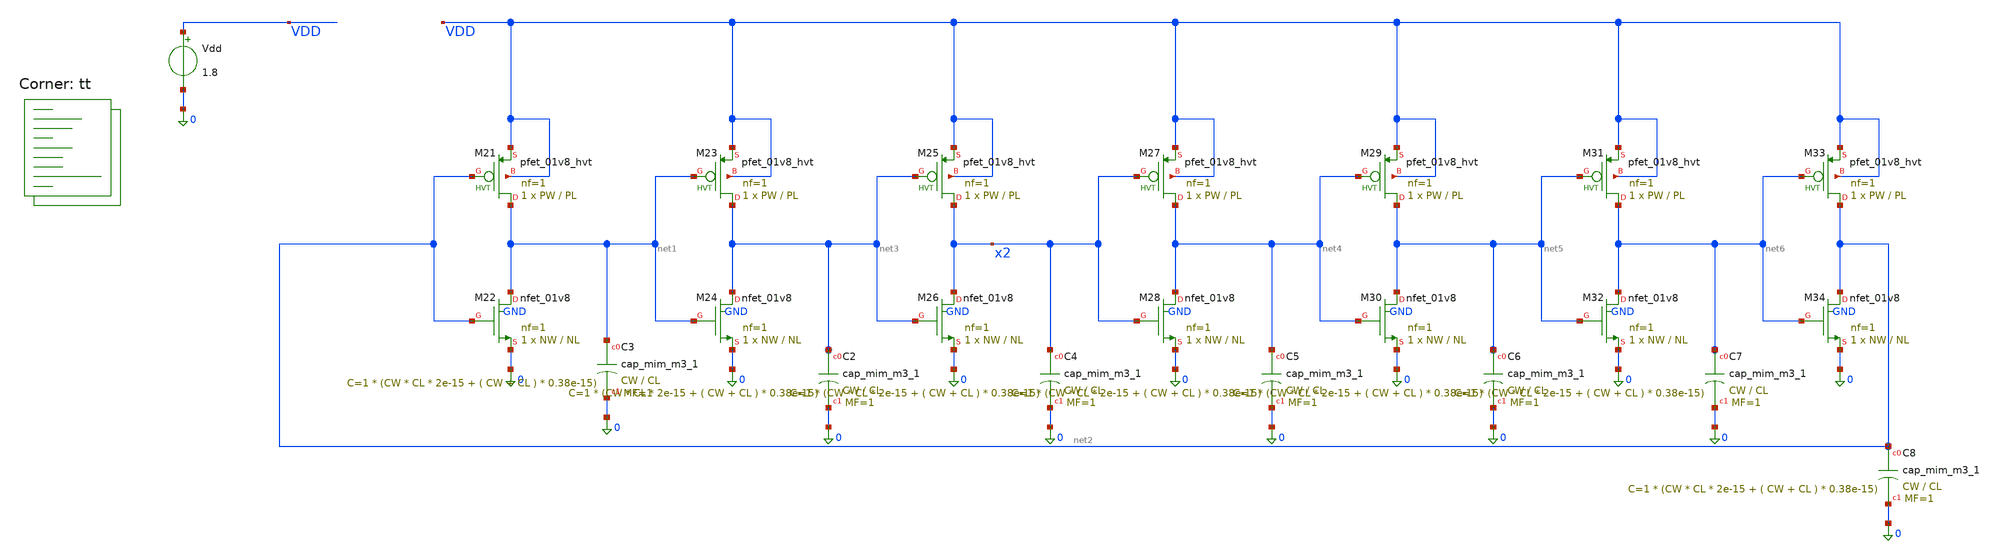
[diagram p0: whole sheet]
** sch_path: schem/ring_osc_trans_analysis_tb.sch
**.subckt ring_osc_trans_analysis_tb
XM21 net1 net2 VDD VDD sky130_fd_pr__pfet_01v8_hvt L=PL W=PW nf=1 ad='int((1 + 1)/2) * PW / 1 * 0.29'
+ as='int((1 + 2)/2) * PW / 1 * 0.29' pd='2*int((1 + 1)/2) * (PW / 1 + 0.29)' ps='2*int((1 + 2)/2) * (PW / 1 + 0.29)'
+ nrd='0.29 / PW ' nrs='0.29 / PW ' sa=0 sb=0 sd=0 mult=1 m=1
XM22 net1 net2 0 GND sky130_fd_pr__nfet_01v8 L=NL W=NW nf=1 ad='int((1 + 1)/2) * NW / 1 * 0.29' as='int((1 + 2)/2) * NW / 1 * 0.29'
+ pd='2*int((1 + 1)/2) * (NW / 1 + 0.29)' ps='2*int((1 + 2)/2) * (NW / 1 + 0.29)' nrd='0.29 / NW ' nrs='0.29 / NW '
+ sa=0 sb=0 sd=0 mult=1 m=1
XM23 net3 net1 VDD VDD sky130_fd_pr__pfet_01v8_hvt L=PL W=PW nf=1 ad='int((1 + 1)/2) * PW / 1 * 0.29'
+ as='int((1 + 2)/2) * PW / 1 * 0.29' pd='2*int((1 + 1)/2) * (PW / 1 + 0.29)' ps='2*int((1 + 2)/2) * (PW / 1 + 0.29)'
+ nrd='0.29 / PW ' nrs='0.29 / PW ' sa=0 sb=0 sd=0 mult=1 m=1
XM24 net3 net1 0 GND sky130_fd_pr__nfet_01v8 L=NL W=NW nf=1 ad='int((1 + 1)/2) * NW / 1 * 0.29' as='int((1 + 2)/2) * NW / 1 * 0.29'
+ pd='2*int((1 + 1)/2) * (NW / 1 + 0.29)' ps='2*int((1 + 2)/2) * (NW / 1 + 0.29)' nrd='0.29 / NW ' nrs='0.29 / NW '
+ sa=0 sb=0 sd=0 mult=1 m=1
XM25 x2 net3 VDD VDD sky130_fd_pr__pfet_01v8_hvt L=PL W=PW nf=1 ad='int((1 + 1)/2) * PW / 1 * 0.29' as='int((1 + 2)/2) * PW / 1 * 0.29'
+ pd='2*int((1 + 1)/2) * (PW / 1 + 0.29)' ps='2*int((1 + 2)/2) * (PW / 1 + 0.29)' nrd='0.29 / PW ' nrs='0.29 / PW '
+ sa=0 sb=0 sd=0 mult=1 m=1
XM26 x2 net3 0 GND sky130_fd_pr__nfet_01v8 L=NL W=NW nf=1 ad='int((1 + 1)/2) * NW / 1 * 0.29' as='int((1 + 2)/2) * NW / 1 * 0.29'
+ pd='2*int((1 + 1)/2) * (NW / 1 + 0.29)' ps='2*int((1 + 2)/2) * (NW / 1 + 0.29)' nrd='0.29 / NW ' nrs='0.29 / NW '
+ sa=0 sb=0 sd=0 mult=1 m=1
XM27 net4 x2 VDD VDD sky130_fd_pr__pfet_01v8_hvt L=PL W=PW nf=1 ad='int((1 + 1)/2) * PW / 1 * 0.29' as='int((1 + 2)/2) * PW / 1 * 0.29'
+ pd='2*int((1 + 1)/2) * (PW / 1 + 0.29)' ps='2*int((1 + 2)/2) * (PW / 1 + 0.29)' nrd='0.29 / PW ' nrs='0.29 / PW '
+ sa=0 sb=0 sd=0 mult=1 m=1
XM28 net4 x2 0 GND sky130_fd_pr__nfet_01v8 L=NL W=NW nf=1 ad='int((1 + 1)/2) * NW / 1 * 0.29' as='int((1 + 2)/2) * NW / 1 * 0.29'
+ pd='2*int((1 + 1)/2) * (NW / 1 + 0.29)' ps='2*int((1 + 2)/2) * (NW / 1 + 0.29)' nrd='0.29 / NW ' nrs='0.29 / NW '
+ sa=0 sb=0 sd=0 mult=1 m=1
XM29 net5 net4 VDD VDD sky130_fd_pr__pfet_01v8_hvt L=PL W=PW nf=1 ad='int((1 + 1)/2) * PW / 1 * 0.29'
+ as='int((1 + 2)/2) * PW / 1 * 0.29' pd='2*int((1 + 1)/2) * (PW / 1 + 0.29)' ps='2*int((1 + 2)/2) * (PW / 1 + 0.29)'
+ nrd='0.29 / PW ' nrs='0.29 / PW ' sa=0 sb=0 sd=0 mult=1 m=1
XM30 net5 net4 0 GND sky130_fd_pr__nfet_01v8 L=NL W=NW nf=1 ad='int((1 + 1)/2) * NW / 1 * 0.29' as='int((1 + 2)/2) * NW / 1 * 0.29'
+ pd='2*int((1 + 1)/2) * (NW / 1 + 0.29)' ps='2*int((1 + 2)/2) * (NW / 1 + 0.29)' nrd='0.29 / NW ' nrs='0.29 / NW '
+ sa=0 sb=0 sd=0 mult=1 m=1
XM31 net6 net5 VDD VDD sky130_fd_pr__pfet_01v8_hvt L=PL W=PW nf=1 ad='int((1 + 1)/2) * PW / 1 * 0.29'
+ as='int((1 + 2)/2) * PW / 1 * 0.29' pd='2*int((1 + 1)/2) * (PW / 1 + 0.29)' ps='2*int((1 + 2)/2) * (PW / 1 + 0.29)'
+ nrd='0.29 / PW ' nrs='0.29 / PW ' sa=0 sb=0 sd=0 mult=1 m=1
XM32 net6 net5 0 GND sky130_fd_pr__nfet_01v8 L=NL W=NW nf=1 ad='int((1 + 1)/2) * NW / 1 * 0.29' as='int((1 + 2)/2) * NW / 1 * 0.29'
+ pd='2*int((1 + 1)/2) * (NW / 1 + 0.29)' ps='2*int((1 + 2)/2) * (NW / 1 + 0.29)' nrd='0.29 / NW ' nrs='0.29 / NW '
+ sa=0 sb=0 sd=0 mult=1 m=1
XM33 net2 net6 VDD VDD sky130_fd_pr__pfet_01v8_hvt L=PL W=PW nf=1 ad='int((1 + 1)/2) * PW / 1 * 0.29'
+ as='int((1 + 2)/2) * PW / 1 * 0.29' pd='2*int((1 + 1)/2) * (PW / 1 + 0.29)' ps='2*int((1 + 2)/2) * (PW / 1 + 0.29)'
+ nrd='0.29 / PW ' nrs='0.29 / PW ' sa=0 sb=0 sd=0 mult=1 m=1
XM34 net2 net6 0 GND sky130_fd_pr__nfet_01v8 L=NL W=NW nf=1 ad='int((1 + 1)/2) * NW / 1 * 0.29' as='int((1 + 2)/2) * NW / 1 * 0.29'
+ pd='2*int((1 + 1)/2) * (NW / 1 + 0.29)' ps='2*int((1 + 2)/2) * (NW / 1 + 0.29)' nrd='0.29 / NW ' nrs='0.29 / NW '
+ sa=0 sb=0 sd=0 mult=1 m=1
Vdd VDD 0 1.8
.save i(vdd)
XC2 net3 0 sky130_fd_pr__cap_mim_m3_1 W=CW L=CL MF=1 m=1
XC3 net1 0 sky130_fd_pr__cap_mim_m3_1 W=CW L=CL MF=1 m=1
XC4 x2 0 sky130_fd_pr__cap_mim_m3_1 W=CW L=CL MF=1 m=1
XC5 net4 0 sky130_fd_pr__cap_mim_m3_1 W=CW L=CL MF=1 m=1
XC6 net5 0 sky130_fd_pr__cap_mim_m3_1 W=CW L=CL MF=1 m=1
XC7 net6 0 sky130_fd_pr__cap_mim_m3_1 W=CW L=CL MF=1 m=1
XC8 net2 0 sky130_fd_pr__cap_mim_m3_1 W=CW L=CL MF=1 m=1
**** begin user architecture code
.lib $::SKYWATER_MODELS/sky130.lib.spice tt



.include slow_osc.save
* 320 MHz : 4f RW=1 PW=1.12 PL=0.45 NW=0.740 NL=0.45
* 250 MHz : 4f PW=1.12 PL=0.5 NW=0.82 NL=0.5
* 260 MHz : 4f PW=0.82 PL=0.5 NW=0.55 NL=0.5
* 100 MHz : 4f PW=1.5 PL=1.0 NW=1.0 NL=1.0
* 18 MHz :  4f PW=7.0 PL=0.25 NW=1.0 NL=8.0
* 30 MHz : CX=64f RW=1 PW=1.5 PL=1.0 NW=1.0 NL=1.0
* 30 MHz : looks clean CX=64f PW=2.0 PL=1.0 NW=1.0 NL=1.0
* version with mim cap CW=6 CL=5 PW=2.0 PL=1.0 NW=1.0 NL=1.0
.param CW=6 CL=5 PW=2.0 PL=1.0 NW=1.0 NL=1.0
.tran 0.02n 200n
.save all
.control
  reset
  run
  write slow_osc.raw
  quit 0
.endc



**** end user architecture code
**.ends
.end
